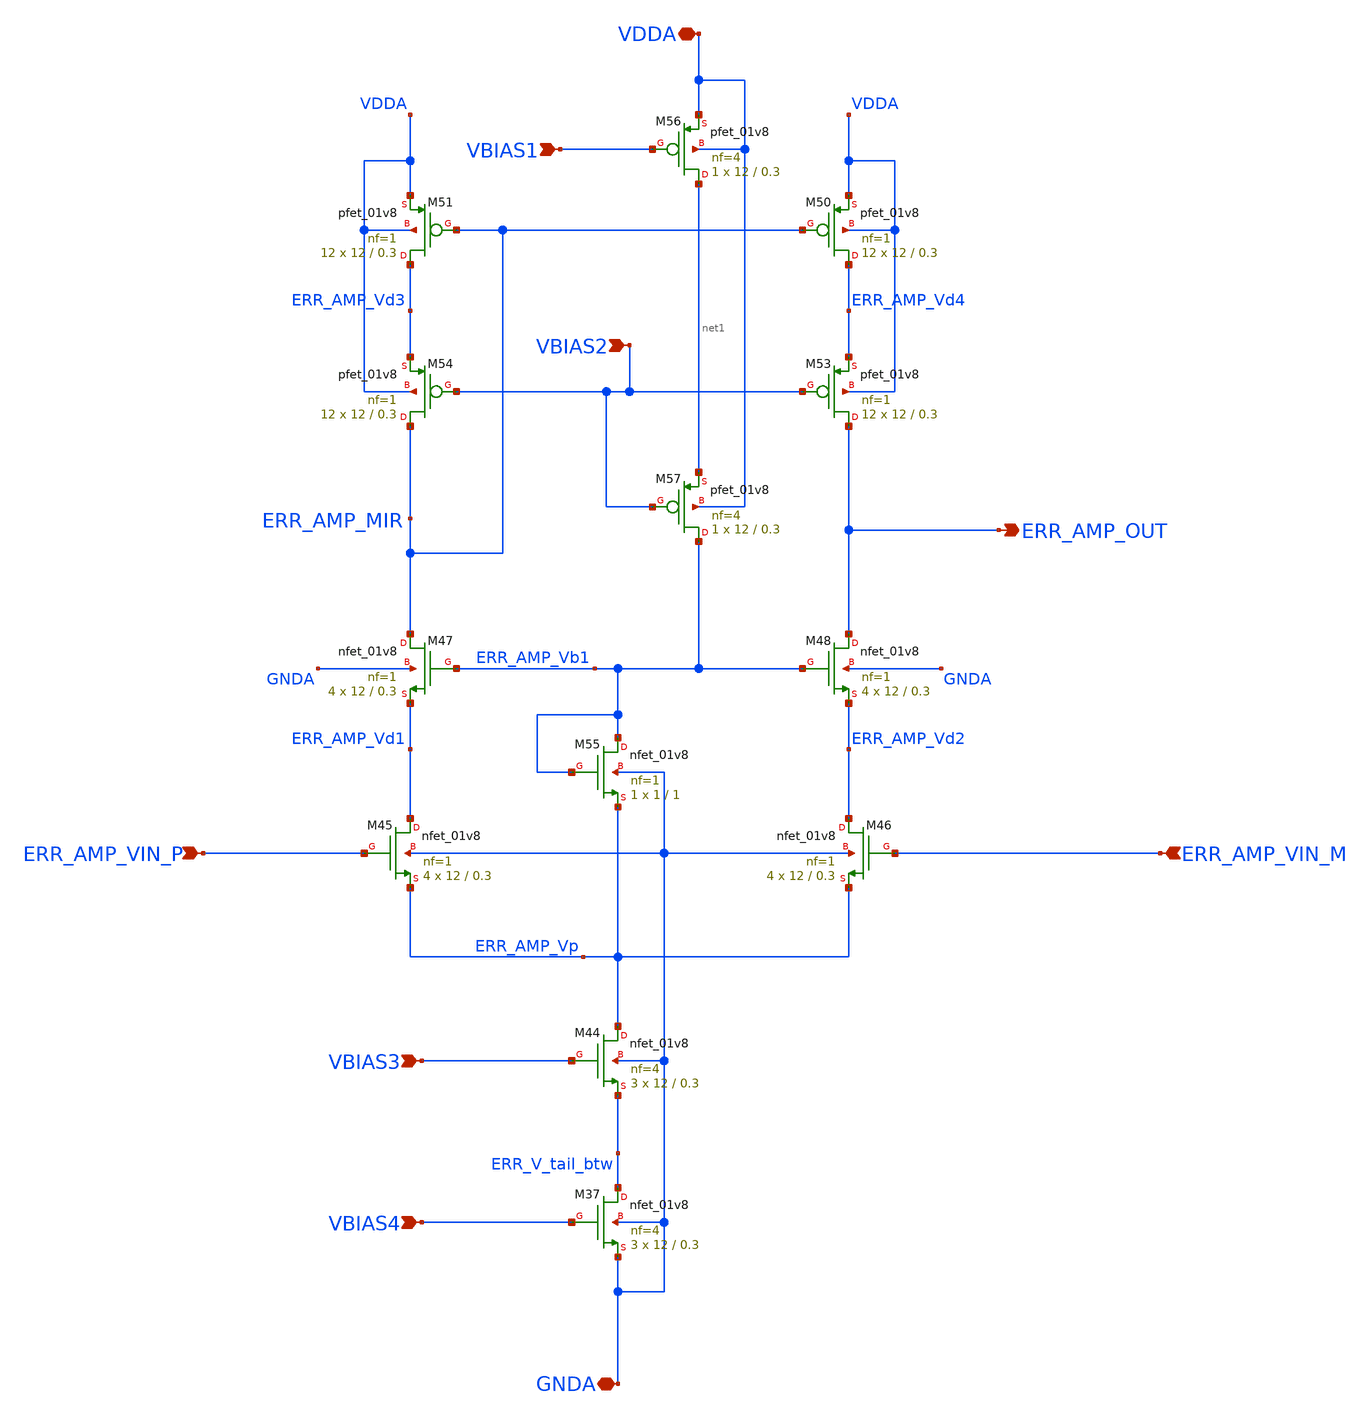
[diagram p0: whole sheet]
** sch_path: projects/ASU/EEE572/schematic/error_opamp.sch
**.subckt error_opamp ERR_AMP_VIN_P ERR_AMP_VIN_M VBIAS4 VBIAS3 VBIAS2 VBIAS1 VDDA GNDA ERR_AMP_OUT
*.ipin ERR_AMP_VIN_P
*.ipin ERR_AMP_VIN_M
*.ipin VBIAS4
*.ipin VBIAS3
*.ipin VBIAS2
*.ipin VBIAS1
*.iopin VDDA
*.iopin GNDA
*.opin ERR_AMP_OUT
XM37 ERR_V_tail_btw VBIAS4 GNDA GNDA sky130_fd_pr__nfet_01v8 L=0.3 W=12 nf=4 ad='int((nf+1)/2) * W/nf * 0.29'
+ as='int((nf+2)/2) * W/nf * 0.29' pd='2*int((nf+1)/2) * (W/nf + 0.29)' ps='2*int((nf+2)/2) * (W/nf + 0.29)'
+ nrd='0.29 / W' nrs='0.29 / W' sa=0 sb=0 sd=0 mult=3 m=3
XM44 ERR_AMP_Vp VBIAS3 ERR_V_tail_btw GNDA sky130_fd_pr__nfet_01v8 L=0.3 W=12 nf=4 ad='int((nf+1)/2) * W/nf * 0.29'
+ as='int((nf+2)/2) * W/nf * 0.29' pd='2*int((nf+1)/2) * (W/nf + 0.29)' ps='2*int((nf+2)/2) * (W/nf + 0.29)'
+ nrd='0.29 / W' nrs='0.29 / W' sa=0 sb=0 sd=0 mult=3 m=3
XM45 ERR_AMP_Vd1 ERR_AMP_VIN_P ERR_AMP_Vp GNDA sky130_fd_pr__nfet_01v8 L=0.3 W=12 nf=1 ad='int((nf+1)/2) * W/nf * 0.29'
+ as='int((nf+2)/2) * W/nf * 0.29' pd='2*int((nf+1)/2) * (W/nf + 0.29)' ps='2*int((nf+2)/2) * (W/nf + 0.29)'
+ nrd='0.29 / W' nrs='0.29 / W' sa=0 sb=0 sd=0 mult=4 m=4
XM46 ERR_AMP_Vd2 ERR_AMP_VIN_M ERR_AMP_Vp GNDA sky130_fd_pr__nfet_01v8 L=0.3 W=12 nf=1 ad='int((nf+1)/2) * W/nf * 0.29'
+ as='int((nf+2)/2) * W/nf * 0.29' pd='2*int((nf+1)/2) * (W/nf + 0.29)' ps='2*int((nf+2)/2) * (W/nf + 0.29)'
+ nrd='0.29 / W' nrs='0.29 / W' sa=0 sb=0 sd=0 mult=4 m=4
XM47 ERR_AMP_MIR ERR_AMP_Vb1 ERR_AMP_Vd1 GNDA sky130_fd_pr__nfet_01v8 L=0.3 W=12 nf=1 ad='int((nf+1)/2) * W/nf * 0.29'
+ as='int((nf+2)/2) * W/nf * 0.29' pd='2*int((nf+1)/2) * (W/nf + 0.29)' ps='2*int((nf+2)/2) * (W/nf + 0.29)'
+ nrd='0.29 / W' nrs='0.29 / W' sa=0 sb=0 sd=0 mult=4 m=4
XM48 ERR_AMP_OUT ERR_AMP_Vb1 ERR_AMP_Vd2 GNDA sky130_fd_pr__nfet_01v8 L=0.3 W=12 nf=1 ad='int((nf+1)/2) * W/nf * 0.29'
+ as='int((nf+2)/2) * W/nf * 0.29' pd='2*int((nf+1)/2) * (W/nf + 0.29)' ps='2*int((nf+2)/2) * (W/nf + 0.29)'
+ nrd='0.29 / W' nrs='0.29 / W' sa=0 sb=0 sd=0 mult=4 m=4
XM50 ERR_AMP_Vd4 ERR_AMP_MIR VDDA VDDA sky130_fd_pr__pfet_01v8 L=0.3 W=12 nf=1 ad='int((nf+1)/2) * W/nf * 0.29'
+ as='int((nf+2)/2) * W/nf * 0.29' pd='2*int((nf+1)/2) * (W/nf + 0.29)' ps='2*int((nf+2)/2) * (W/nf + 0.29)'
+ nrd='0.29 / W' nrs='0.29 / W' sa=0 sb=0 sd=0 mult=12 m=12
XM51 ERR_AMP_Vd3 ERR_AMP_MIR VDDA VDDA sky130_fd_pr__pfet_01v8 L=0.3 W=12 nf=1 ad='int((nf+1)/2) * W/nf * 0.29'
+ as='int((nf+2)/2) * W/nf * 0.29' pd='2*int((nf+1)/2) * (W/nf + 0.29)' ps='2*int((nf+2)/2) * (W/nf + 0.29)'
+ nrd='0.29 / W' nrs='0.29 / W' sa=0 sb=0 sd=0 mult=12 m=12
XM53 ERR_AMP_OUT VBIAS2 ERR_AMP_Vd4 VDDA sky130_fd_pr__pfet_01v8 L=0.3 W=12 nf=1 ad='int((nf+1)/2) * W/nf * 0.29'
+ as='int((nf+2)/2) * W/nf * 0.29' pd='2*int((nf+1)/2) * (W/nf + 0.29)' ps='2*int((nf+2)/2) * (W/nf + 0.29)'
+ nrd='0.29 / W' nrs='0.29 / W' sa=0 sb=0 sd=0 mult=12 m=12
XM54 ERR_AMP_MIR VBIAS2 ERR_AMP_Vd3 VDDA sky130_fd_pr__pfet_01v8 L=0.3 W=12 nf=1 ad='int((nf+1)/2) * W/nf * 0.29'
+ as='int((nf+2)/2) * W/nf * 0.29' pd='2*int((nf+1)/2) * (W/nf + 0.29)' ps='2*int((nf+2)/2) * (W/nf + 0.29)'
+ nrd='0.29 / W' nrs='0.29 / W' sa=0 sb=0 sd=0 mult=12 m=12
XM55 ERR_AMP_Vb1 ERR_AMP_Vb1 ERR_AMP_Vp GNDA sky130_fd_pr__nfet_01v8 L=1 W=1 nf=1 ad='int((nf+1)/2) * W/nf * 0.29'
+ as='int((nf+2)/2) * W/nf * 0.29' pd='2*int((nf+1)/2) * (W/nf + 0.29)' ps='2*int((nf+2)/2) * (W/nf + 0.29)'
+ nrd='0.29 / W' nrs='0.29 / W' sa=0 sb=0 sd=0 mult=1 m=1
XM56 net1 VBIAS1 VDDA VDDA sky130_fd_pr__pfet_01v8 L=0.3 W=12 nf=4 ad='int((nf+1)/2) * W/nf * 0.29' as='int((nf+2)/2) * W/nf * 0.29'
+ pd='2*int((nf+1)/2) * (W/nf + 0.29)' ps='2*int((nf+2)/2) * (W/nf + 0.29)' nrd='0.29 / W' nrs='0.29 / W'
+ sa=0 sb=0 sd=0 mult=1 m=1
XM57 ERR_AMP_Vb1 VBIAS2 net1 VDDA sky130_fd_pr__pfet_01v8 L=0.3 W=12 nf=4 ad='int((nf+1)/2) * W/nf * 0.29'
+ as='int((nf+2)/2) * W/nf * 0.29' pd='2*int((nf+1)/2) * (W/nf + 0.29)' ps='2*int((nf+2)/2) * (W/nf + 0.29)'
+ nrd='0.29 / W' nrs='0.29 / W' sa=0 sb=0 sd=0 mult=1 m=1
**.ends
.end
